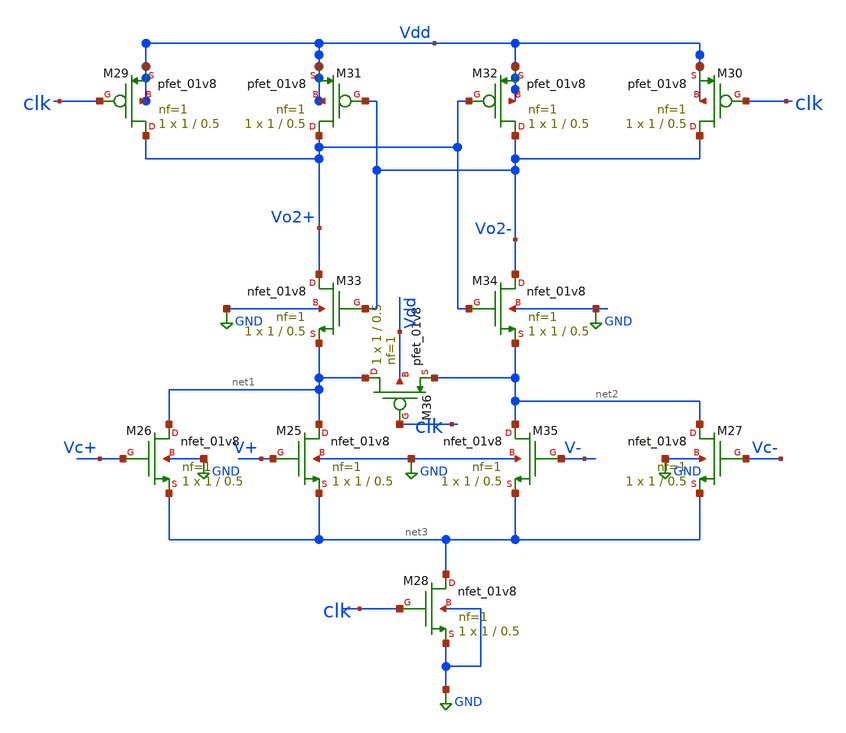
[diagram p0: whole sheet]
** sch_path: xschem/xschemfiles/comparator_layout.sch
**.subckt comparator_layout
XM25 net1 V+ net3 GND sky130_fd_pr__nfet_01v8 L=0.5 W=1 nf=1 ad='int((nf+1)/2) * W/nf * 0.29' as='int((nf+2)/2) * W/nf * 0.29'
+ pd='2*int((nf+1)/2) * (W/nf + 0.29)' ps='2*int((nf+2)/2) * (W/nf + 0.29)' nrd='0.29 / W' nrs='0.29 / W'
+ sa=0 sb=0 sd=0 mult=1 m=1
XM26 net1 Vc+ net3 GND sky130_fd_pr__nfet_01v8 L=0.5 W=1 nf=1 ad='int((nf+1)/2) * W/nf * 0.29' as='int((nf+2)/2) * W/nf * 0.29'
+ pd='2*int((nf+1)/2) * (W/nf + 0.29)' ps='2*int((nf+2)/2) * (W/nf + 0.29)' nrd='0.29 / W' nrs='0.29 / W'
+ sa=0 sb=0 sd=0 mult=1 m=1
XM27 net2 Vc- net3 GND sky130_fd_pr__nfet_01v8 L=0.5 W=1 nf=1 ad='int((nf+1)/2) * W/nf * 0.29' as='int((nf+2)/2) * W/nf * 0.29'
+ pd='2*int((nf+1)/2) * (W/nf + 0.29)' ps='2*int((nf+2)/2) * (W/nf + 0.29)' nrd='0.29 / W' nrs='0.29 / W'
+ sa=0 sb=0 sd=0 mult=1 m=1
XM28 net3 clk GND GND sky130_fd_pr__nfet_01v8 L=0.5 W=1 nf=1 ad='int((nf+1)/2) * W/nf * 0.29' as='int((nf+2)/2) * W/nf * 0.29'
+ pd='2*int((nf+1)/2) * (W/nf + 0.29)' ps='2*int((nf+2)/2) * (W/nf + 0.29)' nrd='0.29 / W' nrs='0.29 / W'
+ sa=0 sb=0 sd=0 mult=1 m=1
XM29 Vo2+ clk Vdd Vdd sky130_fd_pr__pfet_01v8 L=0.5 W=1 nf=1 ad='int((nf+1)/2) * W/nf * 0.29' as='int((nf+2)/2) * W/nf * 0.29'
+ pd='2*int((nf+1)/2) * (W/nf + 0.29)' ps='2*int((nf+2)/2) * (W/nf + 0.29)' nrd='0.29 / W' nrs='0.29 / W'
+ sa=0 sb=0 sd=0 mult=1 m=1
XM30 Vo2- clk Vdd Vdd sky130_fd_pr__pfet_01v8 L=0.5 W=1 nf=1 ad='int((nf+1)/2) * W/nf * 0.29' as='int((nf+2)/2) * W/nf * 0.29'
+ pd='2*int((nf+1)/2) * (W/nf + 0.29)' ps='2*int((nf+2)/2) * (W/nf + 0.29)' nrd='0.29 / W' nrs='0.29 / W'
+ sa=0 sb=0 sd=0 mult=1 m=1
XM31 Vo2+ Vo2- Vdd Vdd sky130_fd_pr__pfet_01v8 L=0.5 W=1 nf=1 ad='int((nf+1)/2) * W/nf * 0.29' as='int((nf+2)/2) * W/nf * 0.29'
+ pd='2*int((nf+1)/2) * (W/nf + 0.29)' ps='2*int((nf+2)/2) * (W/nf + 0.29)' nrd='0.29 / W' nrs='0.29 / W'
+ sa=0 sb=0 sd=0 mult=1 m=1
XM32 Vo2- Vo2+ Vdd Vdd sky130_fd_pr__pfet_01v8 L=0.5 W=1 nf=1 ad='int((nf+1)/2) * W/nf * 0.29' as='int((nf+2)/2) * W/nf * 0.29'
+ pd='2*int((nf+1)/2) * (W/nf + 0.29)' ps='2*int((nf+2)/2) * (W/nf + 0.29)' nrd='0.29 / W' nrs='0.29 / W'
+ sa=0 sb=0 sd=0 mult=1 m=1
XM33 Vo2+ Vo2- net1 GND sky130_fd_pr__nfet_01v8 L=0.5 W=1 nf=1 ad='int((nf+1)/2) * W/nf * 0.29' as='int((nf+2)/2) * W/nf * 0.29'
+ pd='2*int((nf+1)/2) * (W/nf + 0.29)' ps='2*int((nf+2)/2) * (W/nf + 0.29)' nrd='0.29 / W' nrs='0.29 / W'
+ sa=0 sb=0 sd=0 mult=1 m=1
XM34 Vo2- Vo2+ net2 GND sky130_fd_pr__nfet_01v8 L=0.5 W=1 nf=1 ad='int((nf+1)/2) * W/nf * 0.29' as='int((nf+2)/2) * W/nf * 0.29'
+ pd='2*int((nf+1)/2) * (W/nf + 0.29)' ps='2*int((nf+2)/2) * (W/nf + 0.29)' nrd='0.29 / W' nrs='0.29 / W'
+ sa=0 sb=0 sd=0 mult=1 m=1
XM35 net2 V- net3 GND sky130_fd_pr__nfet_01v8 L=0.5 W=1 nf=1 ad='int((nf+1)/2) * W/nf * 0.29' as='int((nf+2)/2) * W/nf * 0.29'
+ pd='2*int((nf+1)/2) * (W/nf + 0.29)' ps='2*int((nf+2)/2) * (W/nf + 0.29)' nrd='0.29 / W' nrs='0.29 / W'
+ sa=0 sb=0 sd=0 mult=1 m=1
XM36 net1 clk net2 Vdd sky130_fd_pr__pfet_01v8 L=0.5 W=1 nf=1 ad='int((nf+1)/2) * W/nf * 0.29' as='int((nf+2)/2) * W/nf * 0.29'
+ pd='2*int((nf+1)/2) * (W/nf + 0.29)' ps='2*int((nf+2)/2) * (W/nf + 0.29)' nrd='0.29 / W' nrs='0.29 / W'
+ sa=0 sb=0 sd=0 mult=1 m=1
**.ends
.GLOBAL GND
.end
